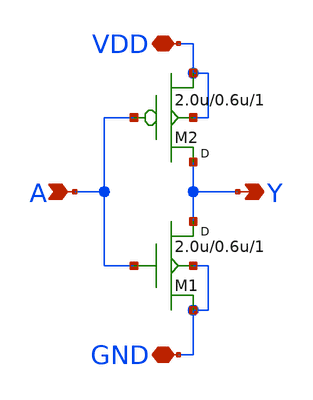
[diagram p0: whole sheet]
** sch_path: Tutorials/1-1_Inverter_XSchem/inverter_TB/inverter.sch
**.subckt inverter A Y VDD GND
*.ipin A
*.opin Y
*.iopin VDD
*.iopin GND
M2 Y A VDD VDD pfet w=2.0u l=0.6u m=1
M1 Y A GND GND nfet w=2.0u l=0.6u m=1
**.ends
.end
